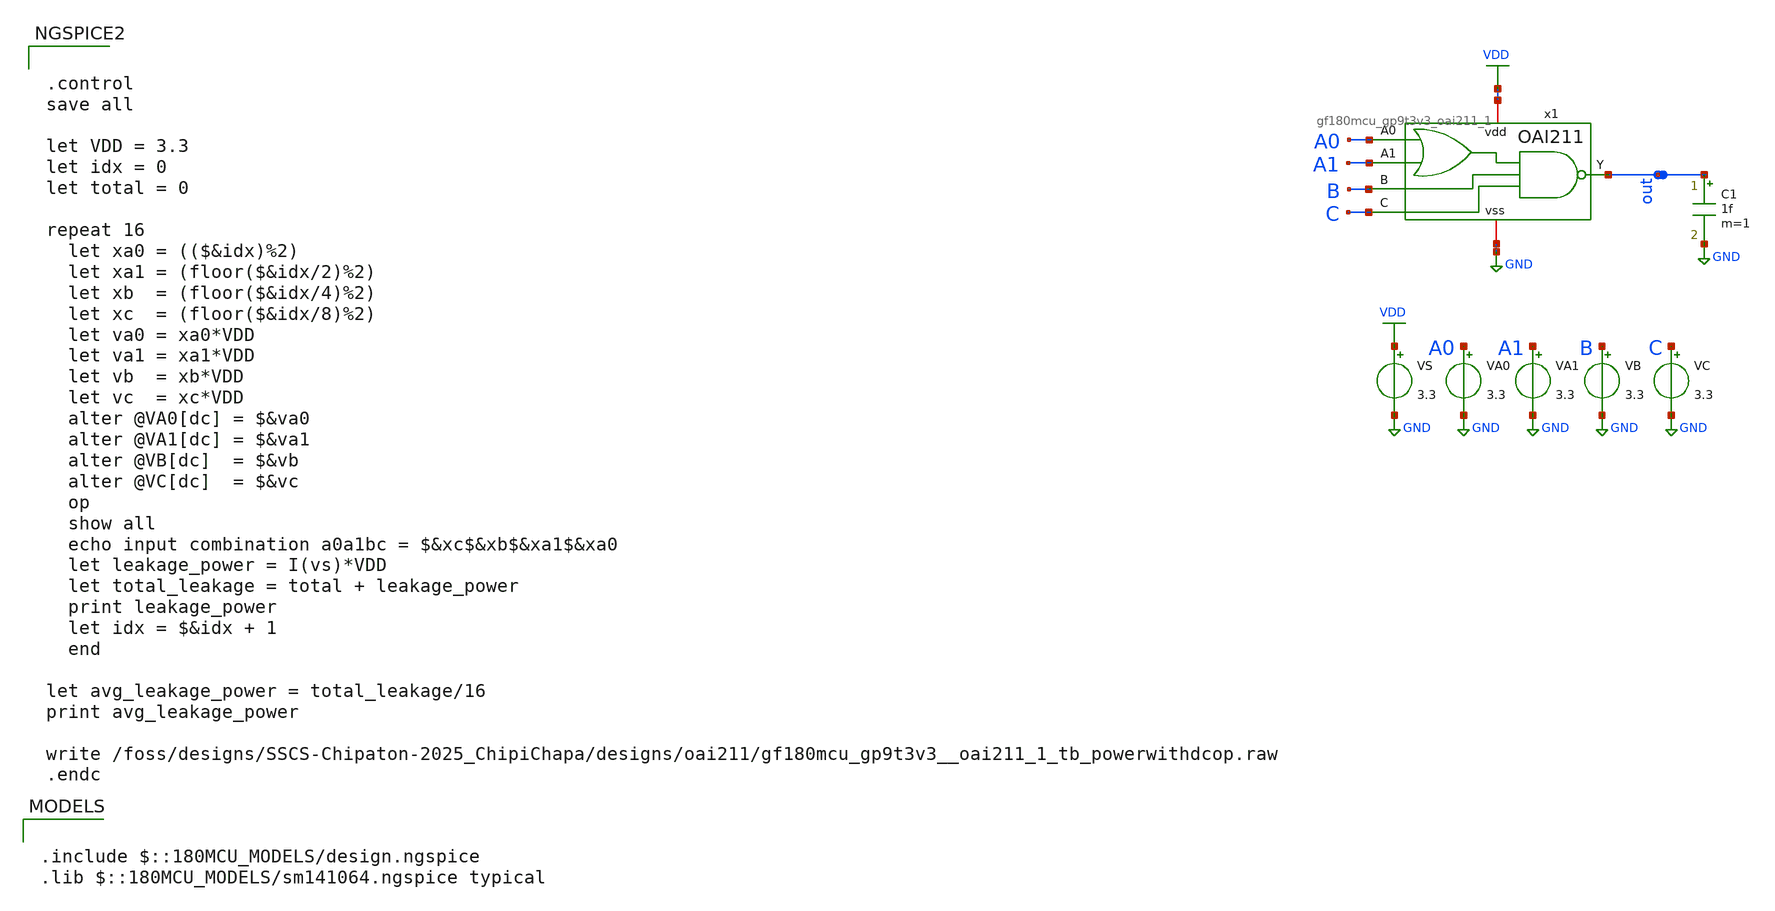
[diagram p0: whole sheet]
** sch_path: designs/oai211/gf180mcu_gp9t3v3_oai211_1_tb_power.sch
**.subckt gf180mcu_gp9t3v3_oai211_1_tb_power
VS VDD GND 3.3
x1 VDD out A0 A1 B C GND gf180mcu_gp9t3v3_oai211_1
VA0 A0 GND 3.3
VA1 A1 GND 3.3
VB B GND 3.3
VC C GND 3.3
C1 out GND 1f m=1
**** begin user architecture code

.include $::180MCU_MODELS/design.ngspice
.lib $::180MCU_MODELS/sm141064.ngspice typical



.control
save all

let VDD = 3.3
let idx = 0
let total = 0

repeat 16
  let xa0 = (($&idx)%2)
  let xa1 = (floor($&idx/2)%2)
  let xb  = (floor($&idx/4)%2)
  let xc  = (floor($&idx/8)%2)
  let va0 = xa0*VDD
  let va1 = xa1*VDD
  let vb  = xb*VDD
  let vc  = xc*VDD
  alter @VA0[dc] = $&va0
  alter @VA1[dc] = $&va1
  alter @VB[dc]  = $&vb
  alter @VC[dc]  = $&vc
  op
  show all
  echo input combination a0a1bc = $&xc$&xb$&xa1$&xa0
  let leakage_power = I(vs)*VDD
  let total_leakage = total + leakage_power
  print leakage_power
  let idx = $&idx + 1
  end

let avg_leakage_power = total_leakage/16
print avg_leakage_power

write
+ /foss/designs/SSCS-Chipaton-2025_ChipiChapa/designs/oai211/gf180mcu_gp9t3v3__oai211_1_tb_powerwithdcop.raw
.endc


**** end user architecture code
**.ends
.GLOBAL VDD
.GLOBAL GND
.end
